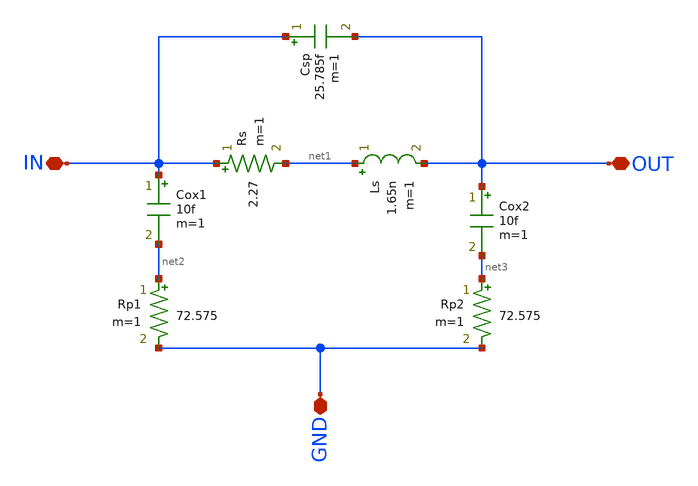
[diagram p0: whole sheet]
** sch_path: Inductance/MODEL_XSCHEM/inductance_1-6nH.sch
**.subckt inductance_1-6nH GND OUT IN
*.iopin GND
*.iopin OUT
*.iopin IN
Ls net1 OUT 1.65n m=1
Cox1 IN net2 10f m=1
Cox2 OUT net3 10f m=1
Csp IN OUT 25.785f m=1
Rp1 net2 GND 72.575 m=1
Rp2 net3 GND 72.575 m=1
Rs IN net1 2.27 m=1
**.ends
.end
